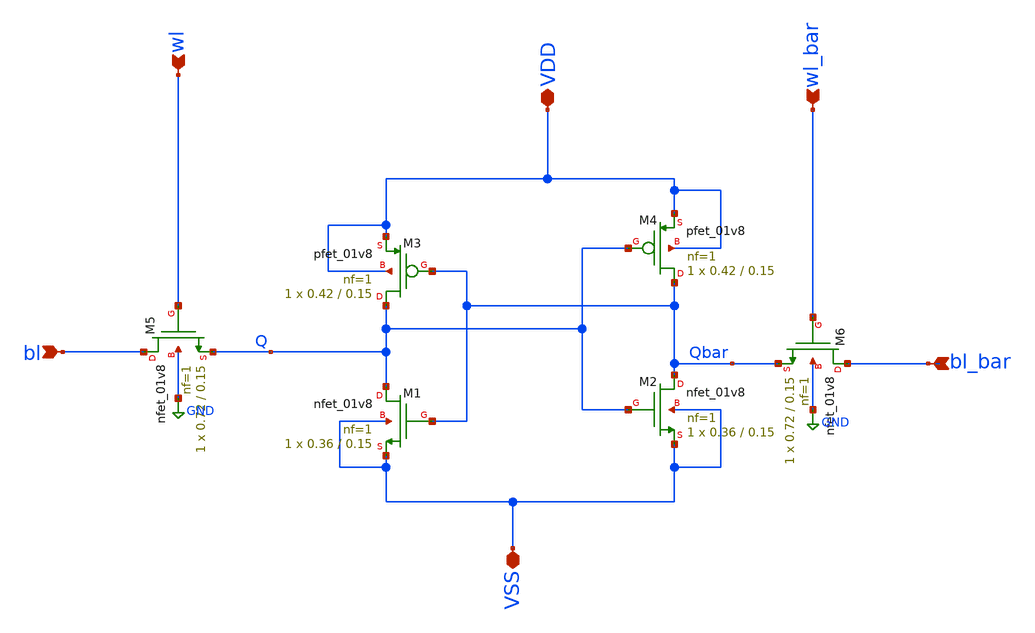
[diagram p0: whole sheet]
** sch_path: nikhil/SRAM/PIM_NOR_long_width.sch
**.subckt PIM_NOR_long_width bl wl VSS VDD wl_bar bl_bar
*.ipin bl
*.ipin wl
*.iopin VSS
*.iopin VDD
*.ipin wl_bar
*.ipin bl_bar
XM2 Qbar Q VSS VSS sky130_fd_pr__nfet_01v8 L=0.15 W=0.36 nf=1 ad='int((nf+1)/2) * W/nf * 0.29' as='int((nf+2)/2) * W/nf * 0.29'
+ pd='2*int((nf+1)/2) * (W/nf + 0.29)' ps='2*int((nf+2)/2) * (W/nf + 0.29)' nrd='0.29 / W' nrs='0.29 / W'
+ sa=0 sb=0 sd=0 mult=1 m=1
XM3 Q Qbar VDD VDD sky130_fd_pr__pfet_01v8 L=0.15 W=0.42 nf=1 ad='int((nf+1)/2) * W/nf * 0.29' as='int((nf+2)/2) * W/nf * 0.29'
+ pd='2*int((nf+1)/2) * (W/nf + 0.29)' ps='2*int((nf+2)/2) * (W/nf + 0.29)' nrd='0.29 / W' nrs='0.29 / W'
+ sa=0 sb=0 sd=0 mult=1 m=1
XM4 Qbar Q VDD VDD sky130_fd_pr__pfet_01v8 L=0.15 W=0.42 nf=1 ad='int((nf+1)/2) * W/nf * 0.29' as='int((nf+2)/2) * W/nf * 0.29'
+ pd='2*int((nf+1)/2) * (W/nf + 0.29)' ps='2*int((nf+2)/2) * (W/nf + 0.29)' nrd='0.29 / W' nrs='0.29 / W'
+ sa=0 sb=0 sd=0 mult=1 m=1
XM5 bl wl Q GND sky130_fd_pr__nfet_01v8 L=0.15 W=0.72 nf=1 ad='int((nf+1)/2) * W/nf * 0.29' as='int((nf+2)/2) * W/nf * 0.29'
+ pd='2*int((nf+1)/2) * (W/nf + 0.29)' ps='2*int((nf+2)/2) * (W/nf + 0.29)' nrd='0.29 / W' nrs='0.29 / W'
+ sa=0 sb=0 sd=0 mult=1 m=1
XM6 bl_bar wl_bar Qbar GND sky130_fd_pr__nfet_01v8 L=0.15 W=0.72 nf=1 ad='int((nf+1)/2) * W/nf * 0.29'
+ as='int((nf+2)/2) * W/nf * 0.29' pd='2*int((nf+1)/2) * (W/nf + 0.29)' ps='2*int((nf+2)/2) * (W/nf + 0.29)'
+ nrd='0.29 / W' nrs='0.29 / W' sa=0 sb=0 sd=0 mult=1 m=1
XM1 Q Qbar VSS VSS sky130_fd_pr__nfet_01v8 L=0.15 W=0.36 nf=1 ad='int((nf+1)/2) * W/nf * 0.29' as='int((nf+2)/2) * W/nf * 0.29'
+ pd='2*int((nf+1)/2) * (W/nf + 0.29)' ps='2*int((nf+2)/2) * (W/nf + 0.29)' nrd='0.29 / W' nrs='0.29 / W'
+ sa=0 sb=0 sd=0 mult=1 m=1
**.ends
.GLOBAL GND
.end
